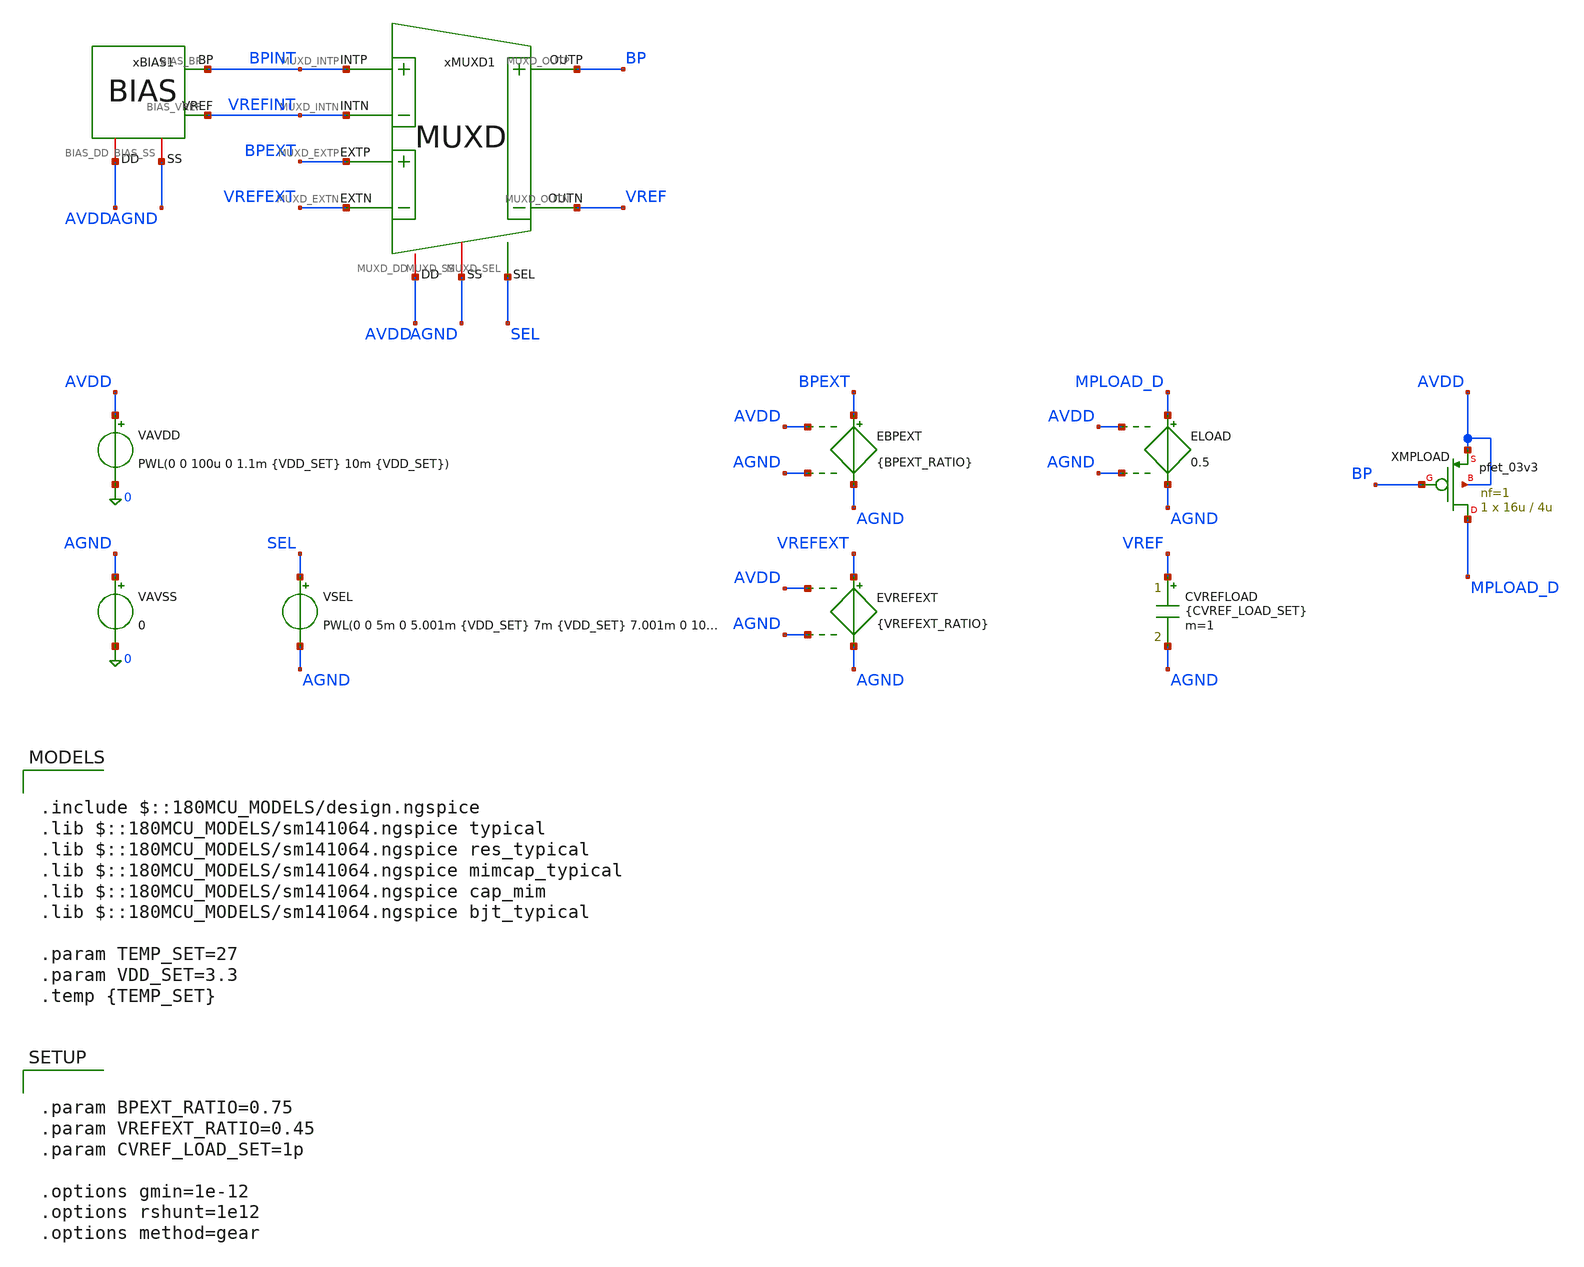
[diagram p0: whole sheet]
** sch_path: Design_Files/IC Design/Testbench/AFE_BLOCKS/BIAS/BIAS_TB_NOM.sch
**.subckt BIAS_TB_NOM
CVREFLOAD VREF AGND {CVREF_LOAD_SET} m=1
VAVDD AVDD 0 PWL(0 0 100u 0 1.1m {VDD_SET} 10m {VDD_SET})
VAVSS AGND 0 0
VSEL SEL AGND PWL(0 0 5m 0 5.001m {VDD_SET} 7m {VDD_SET} 7.001m 0 10m 0)
EBPEXT BPEXT AGND AVDD AGND {BPEXT_RATIO}
EVREFEXT VREFEXT AGND AVDD AGND {VREFEXT_RATIO}
xBIAS1 AVDD AGND BPINT VREFINT BIAS
ELOAD MPLOAD_D AGND AVDD AGND 0.5
XMPLOAD MPLOAD_D BP AVDD AVDD pfet_03v3 L=4u W=16u nf=1 ad='int((nf+1)/2) * W/nf * 0.18u' as='int((nf+2)/2) * W/nf * 0.18u'
+ pd='2*int((nf+1)/2) * (W/nf + 0.18u)' ps='2*int((nf+2)/2) * (W/nf + 0.18u)' nrd='0.18u / W' nrs='0.18u / W'
+ sa=0 sb=0 sd=0 m=1
xMUXD1 AVDD AGND BPINT VREFINT VREF BP BPEXT VREFEXT SEL MUXD
**** begin user architecture code

.include $::180MCU_MODELS/design.ngspice
.lib $::180MCU_MODELS/sm141064.ngspice typical
.lib $::180MCU_MODELS/sm141064.ngspice res_typical
.lib $::180MCU_MODELS/sm141064.ngspice mimcap_typical
.lib $::180MCU_MODELS/sm141064.ngspice cap_mim
.lib $::180MCU_MODELS/sm141064.ngspice bjt_typical

.param TEMP_SET=27
.param VDD_SET=3.3
.temp {TEMP_SET}



.param BPEXT_RATIO=0.75
.param VREFEXT_RATIO=0.45
.param CVREF_LOAD_SET=1p

.options gmin=1e-12
.options rshunt=1e12
.options method=gear





.control

destroy all

set noaskquit
set wr_singlescale
unset wr_vecnames

option klu
option numdgt=15
option method=gear
option maxord=2
option plotwinsize=0

shell mkdir -p
+ /foss/designs/ECG_Acquisition_IC/Measurement_Results/IC_Simulation/AFE_BLOCKS/BIAS/NOM.Result_txt

shell rm -f
+ /foss/designs/ECG_Acquisition_IC/Measurement_Results/IC_Simulation/AFE_BLOCKS/BIAS/NOM.Result_txt/NOM.tran_nom.txt
shell rm -f
+ /foss/designs/ECG_Acquisition_IC/Measurement_Results/IC_Simulation/AFE_BLOCKS/BIAS/NOM.Result_txt/NOM.tran_vl.txt
shell rm -f
+ /foss/designs/ECG_Acquisition_IC/Measurement_Results/IC_Simulation/AFE_BLOCKS/BIAS/NOM.Result_txt/NOM.tran_vh.txt
shell rm -f
+ /foss/designs/ECG_Acquisition_IC/Measurement_Results/IC_Simulation/AFE_BLOCKS/BIAS/NOM.Result_txt/NOM.tran_tl.txt
shell rm -f
+ /foss/designs/ECG_Acquisition_IC/Measurement_Results/IC_Simulation/AFE_BLOCKS/BIAS/NOM.Result_txt/NOM.tran_th.txt
shell rm -f
+ /foss/designs/ECG_Acquisition_IC/Measurement_Results/IC_Simulation/AFE_BLOCKS/BIAS/NOM.Result_txt/NOM.tran_tlvl.txt
shell rm -f
+ /foss/designs/ECG_Acquisition_IC/Measurement_Results/IC_Simulation/AFE_BLOCKS/BIAS/NOM.Result_txt/NOM.tran_thvh.txt
shell rm -f
+ /foss/designs/ECG_Acquisition_IC/Measurement_Results/IC_Simulation/AFE_BLOCKS/BIAS/NOM.Result_txt/NOM.dc2d.txt

alterparam VDD_SET=3.3
alterparam TEMP_SET=27
reset
save all
save @m.xbias1.xmn2.m0[id]
save @m.xbias1.xmst.m0[id]
save @m.xbias1.xmst.m0[vgs]
save @m.xbias1.xmst.m0[vth]

tran 1u 10m

let ibias = abs(eload#branch)
let irs = abs(@m.xbias1.xmn2.m0[id])
let imst = abs(@m.xbias1.xmst.m0[id])
let vgs_mst = @m.xbias1.xmst.m0[vgs]
let vth_mst = @m.xbias1.xmst.m0[vth]
let idd_total = abs(vavdd#branch)
let idd_bias_sel = idd_total-ibias
let power_bias_sel = v(AVDD)*idd_bias_sel

wrdata
+ /foss/designs/ECG_Acquisition_IC/Measurement_Results/IC_Simulation/AFE_BLOCKS/BIAS/NOM.Result_txt/NOM.tran_nom.txt v(AVDD) v(SEL) v(BPINT) v(BP) v(BPEXT) v(VREFINT) v(VREF) v(VREFEXT) ibias irs imst vgs_mst vth_mst
+ idd_bias_sel power_bias_sel

alterparam VDD_SET=3.0
alterparam TEMP_SET=27
reset
save all
save @m.xbias1.xmn2.m0[id]
save @m.xbias1.xmst.m0[id]
save @m.xbias1.xmst.m0[vgs]
save @m.xbias1.xmst.m0[vth]

tran 1u 10m

let ibias = abs(eload#branch)
let irs = abs(@m.xbias1.xmn2.m0[id])
let imst = abs(@m.xbias1.xmst.m0[id])
let vgs_mst = @m.xbias1.xmst.m0[vgs]
let vth_mst = @m.xbias1.xmst.m0[vth]
let idd_total = abs(vavdd#branch)
let idd_bias_sel = idd_total-ibias
let power_bias_sel = v(AVDD)*idd_bias_sel

wrdata
+ /foss/designs/ECG_Acquisition_IC/Measurement_Results/IC_Simulation/AFE_BLOCKS/BIAS/NOM.Result_txt/NOM.tran_vl.txt v(AVDD) v(SEL) v(BPINT) v(BP) v(BPEXT) v(VREFINT) v(VREF) v(VREFEXT) ibias irs imst vgs_mst vth_mst
+ idd_bias_sel power_bias_sel

alterparam VDD_SET=3.6
alterparam TEMP_SET=27
reset
save all
save @m.xbias1.xmn2.m0[id]
save @m.xbias1.xmst.m0[id]
save @m.xbias1.xmst.m0[vgs]
save @m.xbias1.xmst.m0[vth]

tran 1u 10m

let ibias = abs(eload#branch)
let irs = abs(@m.xbias1.xmn2.m0[id])
let imst = abs(@m.xbias1.xmst.m0[id])
let vgs_mst = @m.xbias1.xmst.m0[vgs]
let vth_mst = @m.xbias1.xmst.m0[vth]
let idd_total = abs(vavdd#branch)
let idd_bias_sel = idd_total-ibias
let power_bias_sel = v(AVDD)*idd_bias_sel

wrdata
+ /foss/designs/ECG_Acquisition_IC/Measurement_Results/IC_Simulation/AFE_BLOCKS/BIAS/NOM.Result_txt/NOM.tran_vh.txt v(AVDD) v(SEL) v(BPINT) v(BP) v(BPEXT) v(VREFINT) v(VREF) v(VREFEXT) ibias irs imst vgs_mst vth_mst
+ idd_bias_sel power_bias_sel

alterparam VDD_SET=3.3
alterparam TEMP_SET=-40
reset
save all
save @m.xbias1.xmn2.m0[id]
save @m.xbias1.xmst.m0[id]
save @m.xbias1.xmst.m0[vgs]
save @m.xbias1.xmst.m0[vth]

tran 1u 10m

let ibias = abs(eload#branch)
let irs = abs(@m.xbias1.xmn2.m0[id])
let imst = abs(@m.xbias1.xmst.m0[id])
let vgs_mst = @m.xbias1.xmst.m0[vgs]
let vth_mst = @m.xbias1.xmst.m0[vth]
let idd_total = abs(vavdd#branch)
let idd_bias_sel = idd_total-ibias
let power_bias_sel = v(AVDD)*idd_bias_sel

wrdata
+ /foss/designs/ECG_Acquisition_IC/Measurement_Results/IC_Simulation/AFE_BLOCKS/BIAS/NOM.Result_txt/NOM.tran_tl.txt v(AVDD) v(SEL) v(BPINT) v(BP) v(BPEXT) v(VREFINT) v(VREF) v(VREFEXT) ibias irs imst vgs_mst vth_mst
+ idd_bias_sel power_bias_sel

alterparam VDD_SET=3.3
alterparam TEMP_SET=125
reset
save all
save @m.xbias1.xmn2.m0[id]
save @m.xbias1.xmst.m0[id]
save @m.xbias1.xmst.m0[vgs]
save @m.xbias1.xmst.m0[vth]

tran 1u 10m

let ibias = abs(eload#branch)
let irs = abs(@m.xbias1.xmn2.m0[id])
let imst = abs(@m.xbias1.xmst.m0[id])
let vgs_mst = @m.xbias1.xmst.m0[vgs]
let vth_mst = @m.xbias1.xmst.m0[vth]
let idd_total = abs(vavdd#branch)
let idd_bias_sel = idd_total-ibias
let power_bias_sel = v(AVDD)*idd_bias_sel

wrdata
+ /foss/designs/ECG_Acquisition_IC/Measurement_Results/IC_Simulation/AFE_BLOCKS/BIAS/NOM.Result_txt/NOM.tran_th.txt v(AVDD) v(SEL) v(BPINT) v(BP) v(BPEXT) v(VREFINT) v(VREF) v(VREFEXT) ibias irs imst vgs_mst vth_mst
+ idd_bias_sel power_bias_sel

alterparam VDD_SET=3.0
alterparam TEMP_SET=-40
reset
save all
save @m.xbias1.xmn2.m0[id]
save @m.xbias1.xmst.m0[id]
save @m.xbias1.xmst.m0[vgs]
save @m.xbias1.xmst.m0[vth]

tran 1u 10m

let ibias = abs(eload#branch)
let irs = abs(@m.xbias1.xmn2.m0[id])
let imst = abs(@m.xbias1.xmst.m0[id])
let vgs_mst = @m.xbias1.xmst.m0[vgs]
let vth_mst = @m.xbias1.xmst.m0[vth]
let idd_total = abs(vavdd#branch)
let idd_bias_sel = idd_total-ibias
let power_bias_sel = v(AVDD)*idd_bias_sel

wrdata
+ /foss/designs/ECG_Acquisition_IC/Measurement_Results/IC_Simulation/AFE_BLOCKS/BIAS/NOM.Result_txt/NOM.tran_tlvl.txt v(AVDD) v(SEL) v(BPINT) v(BP) v(BPEXT) v(VREFINT) v(VREF) v(VREFEXT) ibias irs imst vgs_mst vth_mst
+ idd_bias_sel power_bias_sel

alterparam VDD_SET=3.6
alterparam TEMP_SET=125
reset
save all
save @m.xbias1.xmn2.m0[id]
save @m.xbias1.xmst.m0[id]
save @m.xbias1.xmst.m0[vgs]
save @m.xbias1.xmst.m0[vth]

tran 1u 10m

let ibias = abs(eload#branch)
let irs = abs(@m.xbias1.xmn2.m0[id])
let imst = abs(@m.xbias1.xmst.m0[id])
let vgs_mst = @m.xbias1.xmst.m0[vgs]
let vth_mst = @m.xbias1.xmst.m0[vth]
let idd_total = abs(vavdd#branch)
let idd_bias_sel = idd_total-ibias
let power_bias_sel = v(AVDD)*idd_bias_sel

wrdata
+ /foss/designs/ECG_Acquisition_IC/Measurement_Results/IC_Simulation/AFE_BLOCKS/BIAS/NOM.Result_txt/NOM.tran_thvh.txt v(AVDD) v(SEL) v(BPINT) v(BP) v(BPEXT) v(VREFINT) v(VREF) v(VREFEXT) ibias irs imst vgs_mst vth_mst
+ idd_bias_sel power_bias_sel

alterparam VDD_SET=3.3
alterparam TEMP_SET=27
reset
save all
save @m.xbias1.xmn2.m0[id]
save @m.xbias1.xmst.m0[id]
save @m.xbias1.xmst.m0[vgs]
save @m.xbias1.xmst.m0[vth]

dc TEMP -40 125 1 VAVDD 3.0 3.6 0.01

let ibias = abs(eload#branch)
let irs = abs(@m.xbias1.xmn2.m0[id])
let imst = abs(@m.xbias1.xmst.m0[id])
let vgs_mst = @m.xbias1.xmst.m0[vgs]
let vth_mst = @m.xbias1.xmst.m0[vth]
let mst_margin = vth_mst-vgs_mst
let mirror_error = 100*(ibias-irs)/irs
let vref_error = v(VREF)-v(AVDD)/2
let idd_total = abs(vavdd#branch)
let idd_bias_sel = idd_total-ibias
let power_bias_sel = v(AVDD)*idd_bias_sel

wrdata
+ /foss/designs/ECG_Acquisition_IC/Measurement_Results/IC_Simulation/AFE_BLOCKS/BIAS/NOM.Result_txt/NOM.dc2d.txt v(AVDD) v(BPINT) v(BP) v(VREFINT) v(VREF) ibias irs mirror_error vref_error imst mst_margin
+ idd_bias_sel power_bias_sel

quit

.endc


**** end user architecture code
**.ends

* expanding   symbol:  ECG_Acquisition_IC/Design_Files/IC Design/Schematic/AFE_BLOCKS/BIAS/BIAS.sym
*+ # of pins=4
** sym_path: Design_Files/IC Design/Schematic/BIAS/BIAS.sym
** sch_path: Design_Files/IC Design/Schematic/BIAS/BIAS.sch
.subckt BIAS BIAS_DD BIAS_SS BIAS_BP BIAS_VREF
*.iopin BIAS_DD
*.iopin BIAS_SS
*.opin BIAS_BP
*.opin BIAS_VREF
XMN2 BIAS_BP net2 net1 BIAS_SS nfet_03v3 L=4u W=16u nf=1 ad='int((nf+1)/2) * W/nf * 0.18u' as='int((nf+2)/2) * W/nf * 0.18u'
+ pd='2*int((nf+1)/2) * (W/nf + 0.18u)' ps='2*int((nf+2)/2) * (W/nf + 0.18u)' nrd='0.18u / W' nrs='0.18u / W'
+ sa=0 sb=0 sd=0 m=1
XMP2 BIAS_BP BIAS_BP BIAS_DD BIAS_DD pfet_03v3 L=4u W=16u nf=1 ad='int((nf+1)/2) * W/nf * 0.18u' as='int((nf+2)/2) * W/nf * 0.18u'
+ pd='2*int((nf+1)/2) * (W/nf + 0.18u)' ps='2*int((nf+2)/2) * (W/nf + 0.18u)' nrd='0.18u / W' nrs='0.18u / W'
+ sa=0 sb=0 sd=0 m=1
XMN1 net2 net2 net3 BIAS_SS nfet_03v3 L=4u W=24u nf=1 ad='int((nf+1)/2) * W/nf * 0.18u' as='int((nf+2)/2) * W/nf * 0.18u'
+ pd='2*int((nf+1)/2) * (W/nf + 0.18u)' ps='2*int((nf+2)/2) * (W/nf + 0.18u)' nrd='0.18u / W' nrs='0.18u / W'
+ sa=0 sb=0 sd=0 m=1
XMP1 net2 BIAS_BP BIAS_DD BIAS_DD pfet_03v3 L=4u W=16u nf=1 ad='int((nf+1)/2) * W/nf * 0.18u' as='int((nf+2)/2) * W/nf * 0.18u'
+ pd='2*int((nf+1)/2) * (W/nf + 0.18u)' ps='2*int((nf+2)/2) * (W/nf + 0.18u)' nrd='0.18u / W' nrs='0.18u / W'
+ sa=0 sb=0 sd=0 m=1
XMST BIAS_BP BIAS_BP net2 BIAS_SS nfet_03v3 L=10u W=0.5u nf=1 ad='int((nf+1)/2) * W/nf * 0.18u' as='int((nf+2)/2) * W/nf * 0.18u'
+ pd='2*int((nf+1)/2) * (W/nf + 0.18u)' ps='2*int((nf+2)/2) * (W/nf + 0.18u)' nrd='0.18u / W' nrs='0.18u / W'
+ sa=0 sb=0 sd=0 m=1
XRP BIAS_VREF BIAS_DD BIAS_SS ppolyf_u_2k r_width=4e-6 r_length=1000e-6 m=1
XRN BIAS_SS BIAS_VREF BIAS_SS ppolyf_u_2k r_width=4e-6 r_length=1000e-6 m=1
XCN BIAS_VREF BIAS_SS cap_mim_2f0fF c_width=70.7e-6 c_length=70.7e-6 m=1
XQ1 BIAS_SS BIAS_SS net3 pnp_05p00x00p42 m=1 par=1
XQ2 BIAS_SS BIAS_SS net4 pnp_05p00x00p42 m=30 par=30
XRS net4 net1 BIAS_SS nwell r_width=3e-6 r_length=1.522e-6 m=1
.ends


* expanding   symbol:  ECG_Acquisition_IC/Design_Files/IC
*+ Design/Schematic/DIGITAL_BLOCKS/MUXD/MUXD.sym # of pins=9
** sym_path: Design_Files/IC Design/Schematic/DIGITAL_BLOCKS/MUXD/MUXD.sym
** sch_path: Design_Files/IC Design/Schematic/DIGITAL_BLOCKS/MUXD/MUXD.sch
.subckt MUXD MUXD_DD MUXD_SS MUXD_INTP MUXD_INTN MUXD_OUTN MUXD_OUTP MUXD_EXTP MUXD_EXTN MUXD_SEL
*.iopin MUXD_DD
*.iopin MUXD_SS
*.ipin MUXD_INTP
*.ipin MUXD_INTN
*.iopin MUXD_OUTP
*.iopin MUXD_OUTN
*.ipin MUXD_EXTP
*.ipin MUXD_EXTN
*.ipin MUXD_SEL
xINV1 MUXD_DD MUXD_SS MUXD_SEL MUXD_SELB INV
xTG1 MUXD_DD MUXD_SS MUXD_EXTP MUXD_OUTP MUXD_SEL MUXD_SELB TG
xTG2 MUXD_DD MUXD_SS MUXD_INTP MUXD_OUTP MUXD_SELB MUXD_SEL TG
xTG3 MUXD_DD MUXD_SS MUXD_EXTN MUXD_OUTN MUXD_SEL MUXD_SELB TG
xTG4 MUXD_DD MUXD_SS MUXD_INTN MUXD_OUTN MUXD_SELB MUXD_SEL TG
.ends


* expanding   symbol:  ECG_Acquisition_IC/Design_Files/IC
*+ Design/Schematic/DIGITAL_BLOCKS/INV/INV.sym # of pins=4
** sym_path: Design_Files/IC Design/Schematic/INV/INV.sym
** sch_path: Design_Files/IC Design/Schematic/INV/INV.sch
.subckt INV INV_DD INV_SS INV_IN INV_OUT
*.iopin INV_DD
*.iopin INV_SS
*.ipin INV_IN
*.opin INV_OUT
XMINVP INV_OUT INV_IN INV_DD INV_DD pfet_03v3 L=0.5u W=2u nf=1 ad='int((nf+1)/2) * W/nf * 0.18u' as='int((nf+2)/2) * W/nf * 0.18u'
+ pd='2*int((nf+1)/2) * (W/nf + 0.18u)' ps='2*int((nf+2)/2) * (W/nf + 0.18u)' nrd='0.18u / W' nrs='0.18u / W'
+ sa=0 sb=0 sd=0 m=1
XMINVN INV_OUT INV_IN INV_SS INV_SS nfet_03v3 L=0.5u W=1u nf=1 ad='int((nf+1)/2) * W/nf * 0.18u' as='int((nf+2)/2) * W/nf * 0.18u'
+ pd='2*int((nf+1)/2) * (W/nf + 0.18u)' ps='2*int((nf+2)/2) * (W/nf + 0.18u)' nrd='0.18u / W' nrs='0.18u / W'
+ sa=0 sb=0 sd=0 m=1
.ends


* expanding   symbol:  ECG_Acquisition_IC/Design_Files/IC Design/Schematic/DIGITAL_BLOCKS/TG/TG.sym
*+ # of pins=6
** sym_path: Design_Files/IC Design/Schematic/TG/TG.sym
** sch_path: Design_Files/IC Design/Schematic/TG/TG.sch
.subckt TG TG_DD TG_SS TG_A TG_B TG_SEL TG_SELB
*.iopin TG_DD
*.iopin TG_SS
*.iopin TG_A
*.iopin TG_B
*.ipin TG_SEL
*.ipin TG_SELB
XMTGP TG_B TG_SELB TG_A TG_DD pfet_03v3 L=0.5u W=40u nf=1 ad='int((nf+1)/2) * W/nf * 0.18u' as='int((nf+2)/2) * W/nf * 0.18u'
+ pd='2*int((nf+1)/2) * (W/nf + 0.18u)' ps='2*int((nf+2)/2) * (W/nf + 0.18u)' nrd='0.18u / W' nrs='0.18u / W'
+ sa=0 sb=0 sd=0 m=1
XMTGN TG_A TG_SEL TG_B TG_SS nfet_03v3 L=0.5u W=20u nf=1 ad='int((nf+1)/2) * W/nf * 0.18u' as='int((nf+2)/2) * W/nf * 0.18u'
+ pd='2*int((nf+1)/2) * (W/nf + 0.18u)' ps='2*int((nf+2)/2) * (W/nf + 0.18u)' nrd='0.18u / W' nrs='0.18u / W'
+ sa=0 sb=0 sd=0 m=1
.ends

.end
